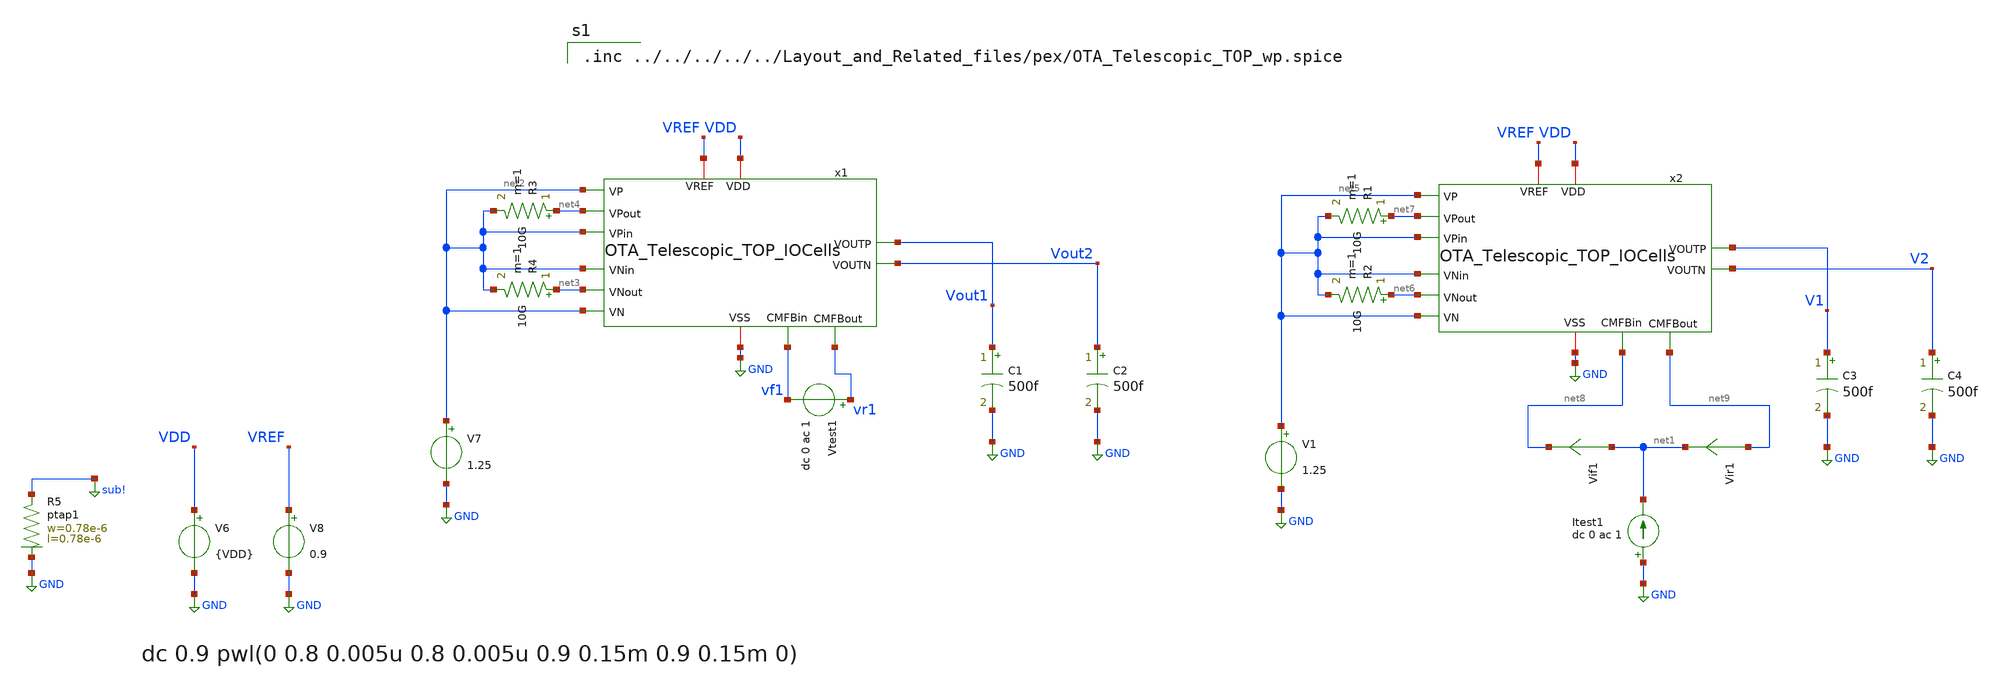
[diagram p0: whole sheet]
** sch_path: OTA_Telescopic/AutoTestbench/tb/done/OTA_Telescopic_TOP_TB_CMFB_io.sch
**.subckt OTA_Telescopic_TOP_TB_CMFB_io
V7 net2 GND 1.25
C1 Vout1 GND 500f m=1
C2 Vout2 GND 500f m=1
V6 VDD GND {VDD}
V8 VREF GND 0.9
Vtest1 vr1 vf1 dc 0 ac 1
Vif1 net1 net8 0
.save i(vif1)
Vir1 net9 net1 0
.save i(vir1)
Itest1 GND net1 dc 0 ac 1
R3 net4 net2 10G m=1
R4 net3 net2 10G m=1
V1 net5 GND 1.25
C3 V1 GND 500f m=1
C4 V2 GND 500f m=1
R1 net7 net5 10G m=1
R2 net6 net5 10G m=1
XR5 sub! GND ptap1 R=262.8 w=0.78e-6 l=0.78e-6
x1 VDD GND net4 net2 net2 Vout2 Vout1 net2 net3 net2 VREF vf1 vr1 OTA_Telescopic_TOP_IOCells
x2 VDD GND net7 net5 net5 V2 V1 net5 net6 net5 VREF net8 net9 OTA_Telescopic_TOP_IOCells
**** begin user architecture code


** opencircuitdesign pdks install
.lib cornerMOSlv.lib mos_$PROCESS
.lib cornerRES.lib res_typ
.lib cornerCAP.lib cap_typ
.temp $TEMP




*.nodeset v(Vout1)=0.9 v(Vout2)=0.9
.options savecurrents reltol=1e-3 abstol=1e-12 gmin=1e-15
.param VDD=$VDD
.control
save VN VP Vout1 Vout2 vr1 vf1 vir1 vif1
set color0 = white

* AC Analysis
ac dec 10 1 5G
remzerovec
write Middlebrook.raw
set appendwrite

* Middlebrook's Method
let tv=-v(vr1)/v(vf1)
let ti=-i(vir1)/i(vif1)
let tmb=(tv*ti - 1)/(tv + ti + 2)

let Av = db(tmb)
meas ac Ao MAX Av
let ABW = Ao-3
meas ac BW WHEN Av=ABW
meas ac UGBW WHEN Av=0

* Phase margin (PM)
let phase_vec= 180/pi*cph(tmb)
meas ac phase FIND phase_vec WHEN frequency=UGBW
let PM = phase+180
print PM

* Gain margin (GM)
meas ac freq180 FIND frequency WHEN phase_vec=-180
meas ac gain FIND Av WHEN frequency=freq180
let GM = 0-gain
print GM

plot Av ylabel 'Magnitude - Middlebrook'
plot phase_vec ylabel 'Phase - Middlebrook'

write Middlebrook_.raw

wrdata CMFB_Av.txt Av
wrdata CMFB_Phase.txt phase_vec
let A0_ = Ao

echo PM $&PM > results.txt
echo A0 $&A0_ >> results.txt


*quit

.endc




.include sg13g2_bondpad.lib
.include diodes.lib
.lib cornerMOShv.lib mos_tt



.inc ../../../../../Layout_and_Related_files/pex/OTA_Telescopic_TOP_wp.spice

**** end user architecture code
**.ends
.GLOBAL GND
.GLOBAL sub!
.end
